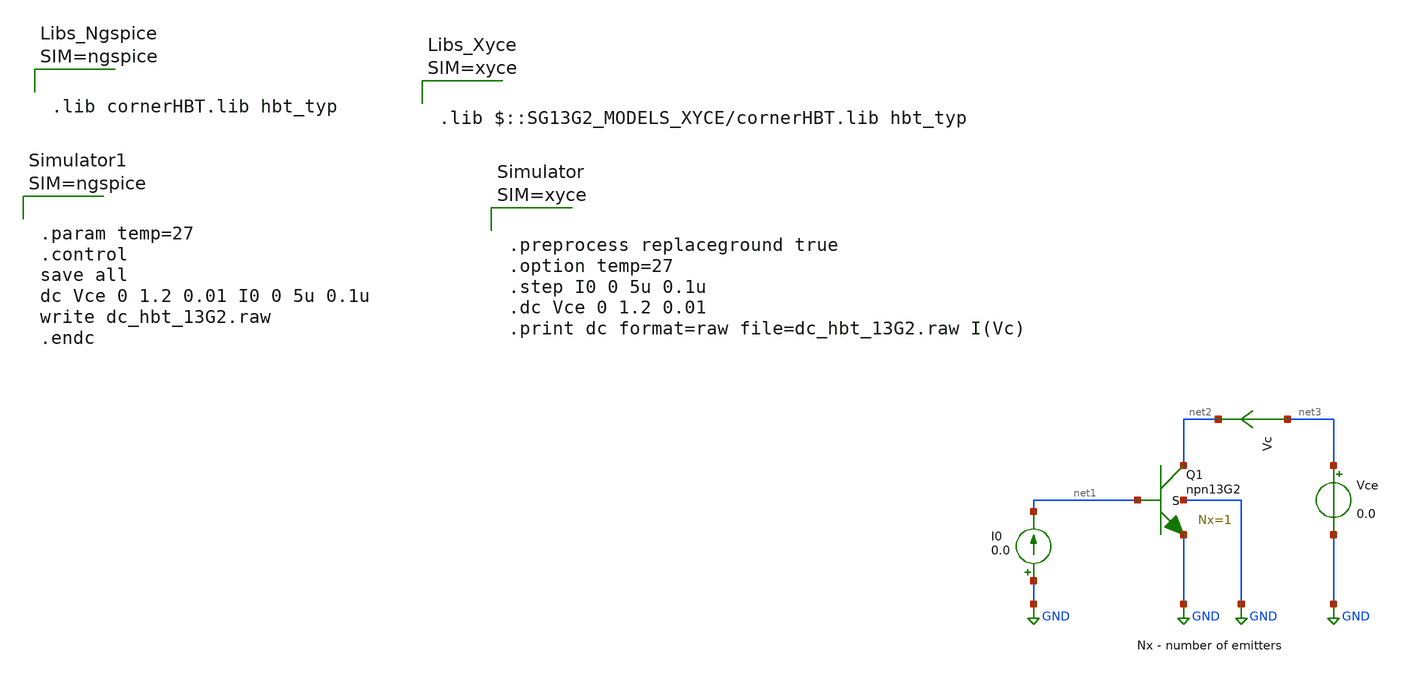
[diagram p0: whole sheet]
** sch_path: ihp-sg13g2/libs.tech/xschem/sg13g2_tests_xyce/dc_hbt_13g2.sch
* Copyright 2023 IHP PDK Authors
**.subckt dc_hbt_13g2
Vce net3 GND 0.0
I0 GND net1 0.0
Vc net3 net2 0
.save i(vc)
XQ1 net2 net1 GND GND npn13G2 Nx=1 mm_ok=1
**** begin user architecture code









.lib cornerHBT.lib hbt_typ






.param temp=27
.control
save all
dc Vce 0 1.2 0.01 I0 0 5u 0.1u
write dc_hbt_13G2.raw
.endc



**** end user architecture code
**.ends
.GLOBAL GND
.end
